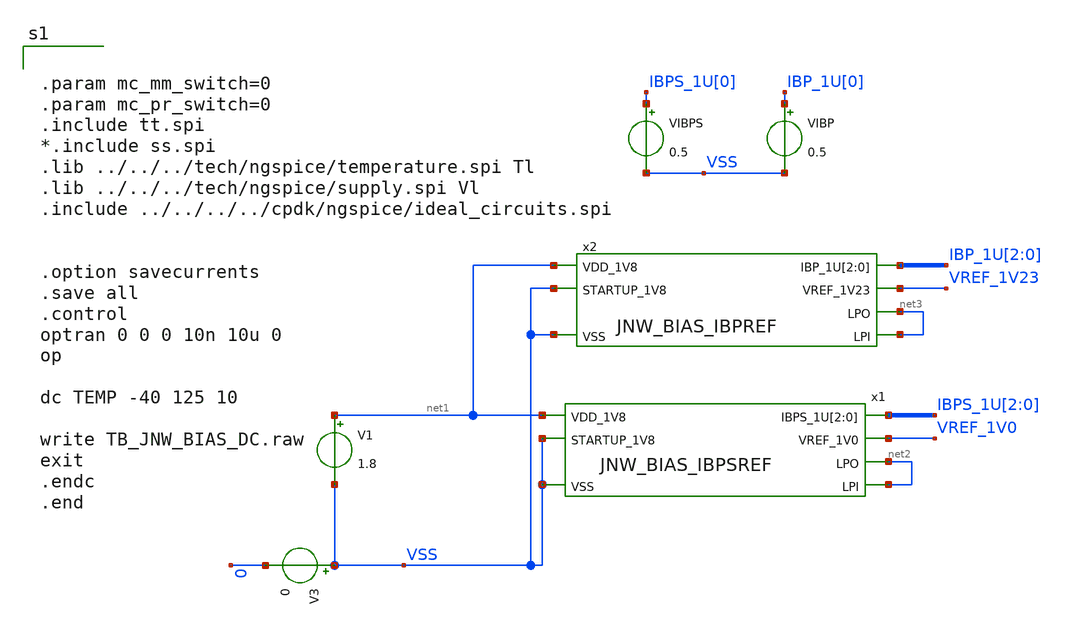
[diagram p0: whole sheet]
** sch_path: design/JNW_BIAS_SKY130A/TB_JNW_BIAS_DC.sch
**.subckt TB_JNW_BIAS_DC
V1 net1 VSS 1.8
VIBPS IBPS_1U[0] VSS 0.5
V3 VSS 0 0
x1 IBPS_1U[2] IBPS_1U[1] IBPS_1U[0] net1 net2 VSS VREF_1V0 net2 VSS JNW_BIAS_IBPSREF
x2 IBP_1U[2] IBP_1U[1] IBP_1U[0] net1 net3 VSS VREF_1V23 net3 VSS JNW_BIAS_IBPREF
VIBP IBP_1U[0] VSS 0.5
**** begin user architecture code


.param mc_mm_switch=0
.param mc_pr_switch=0
.include tt.spi
*.include ss.spi
.lib ../../../tech/ngspice/temperature.spi Tl
.lib ../../../tech/ngspice/supply.spi Vl
.include ../../../../cpdk/ngspice/ideal_circuits.spi


.option savecurrents
.save all
.control
optran 0 0 0 10n 10u 0
op

dc TEMP -40 125 10

write TB_JNW_BIAS_DC.raw
exit
.endc
.end



**** end user architecture code
**.ends
.end
